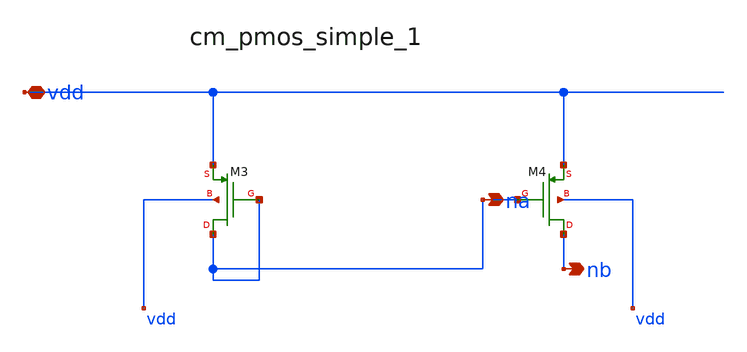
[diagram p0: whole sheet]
** sch_path: analog-db/raw/amp_033_ti_ldo_ref_selfbias/hier/blocks/cm_pmos_simple_1.sch
**.subckt cm_pmos_simple_1 vdd na nb
*.iopin vdd
*.opin na
*.opin nb
XM3 na na vdd vdd sg13_lv_pmos w=x_dut_xm3_w l=x_dut_xm3_l ng=1 m=1
XM4 nb na vdd vdd sg13_lv_pmos w=x_dut_xm4_w l=x_dut_xm4_l ng=1 m=1
**.ends
.end
